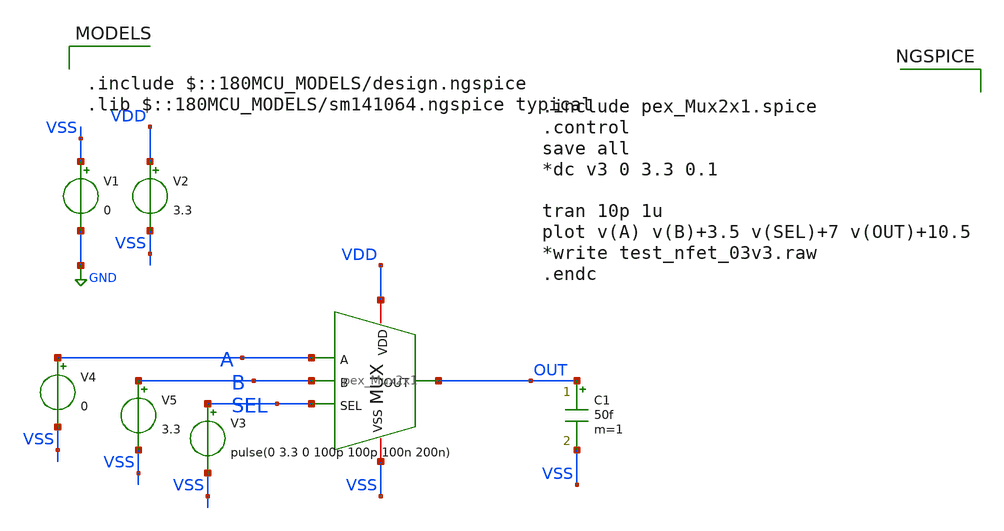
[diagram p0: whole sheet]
** sch_path: DAC_PAKISTAN_01/Pakistan1_Xschem/MUX_TB.sch
**.subckt MUX_TB
V1 VSS GND 0
V2 VDD VSS 3.3
V3 SEL VSS pulse(0 3.3 0 100p 100p 100n 200n)
C1 OUT VSS 50f m=1
V4 A VSS 0
V5 B VSS 3.3
x1 VDD VSS A B SEL OUT pex_Mux2x1
**** begin user architecture code

.include $::180MCU_MODELS/design.ngspice
.lib $::180MCU_MODELS/sm141064.ngspice typical



.include pex_Mux2x1.spice
.control
save all
*dc v3 0 3.3 0.1

tran 10p 1u
plot v(A) v(B)+3.5 v(SEL)+7 v(OUT)+10.5
*write test_nfet_03v3.raw
.endc


**** end user architecture code
**.ends
.GLOBAL GND
.end
